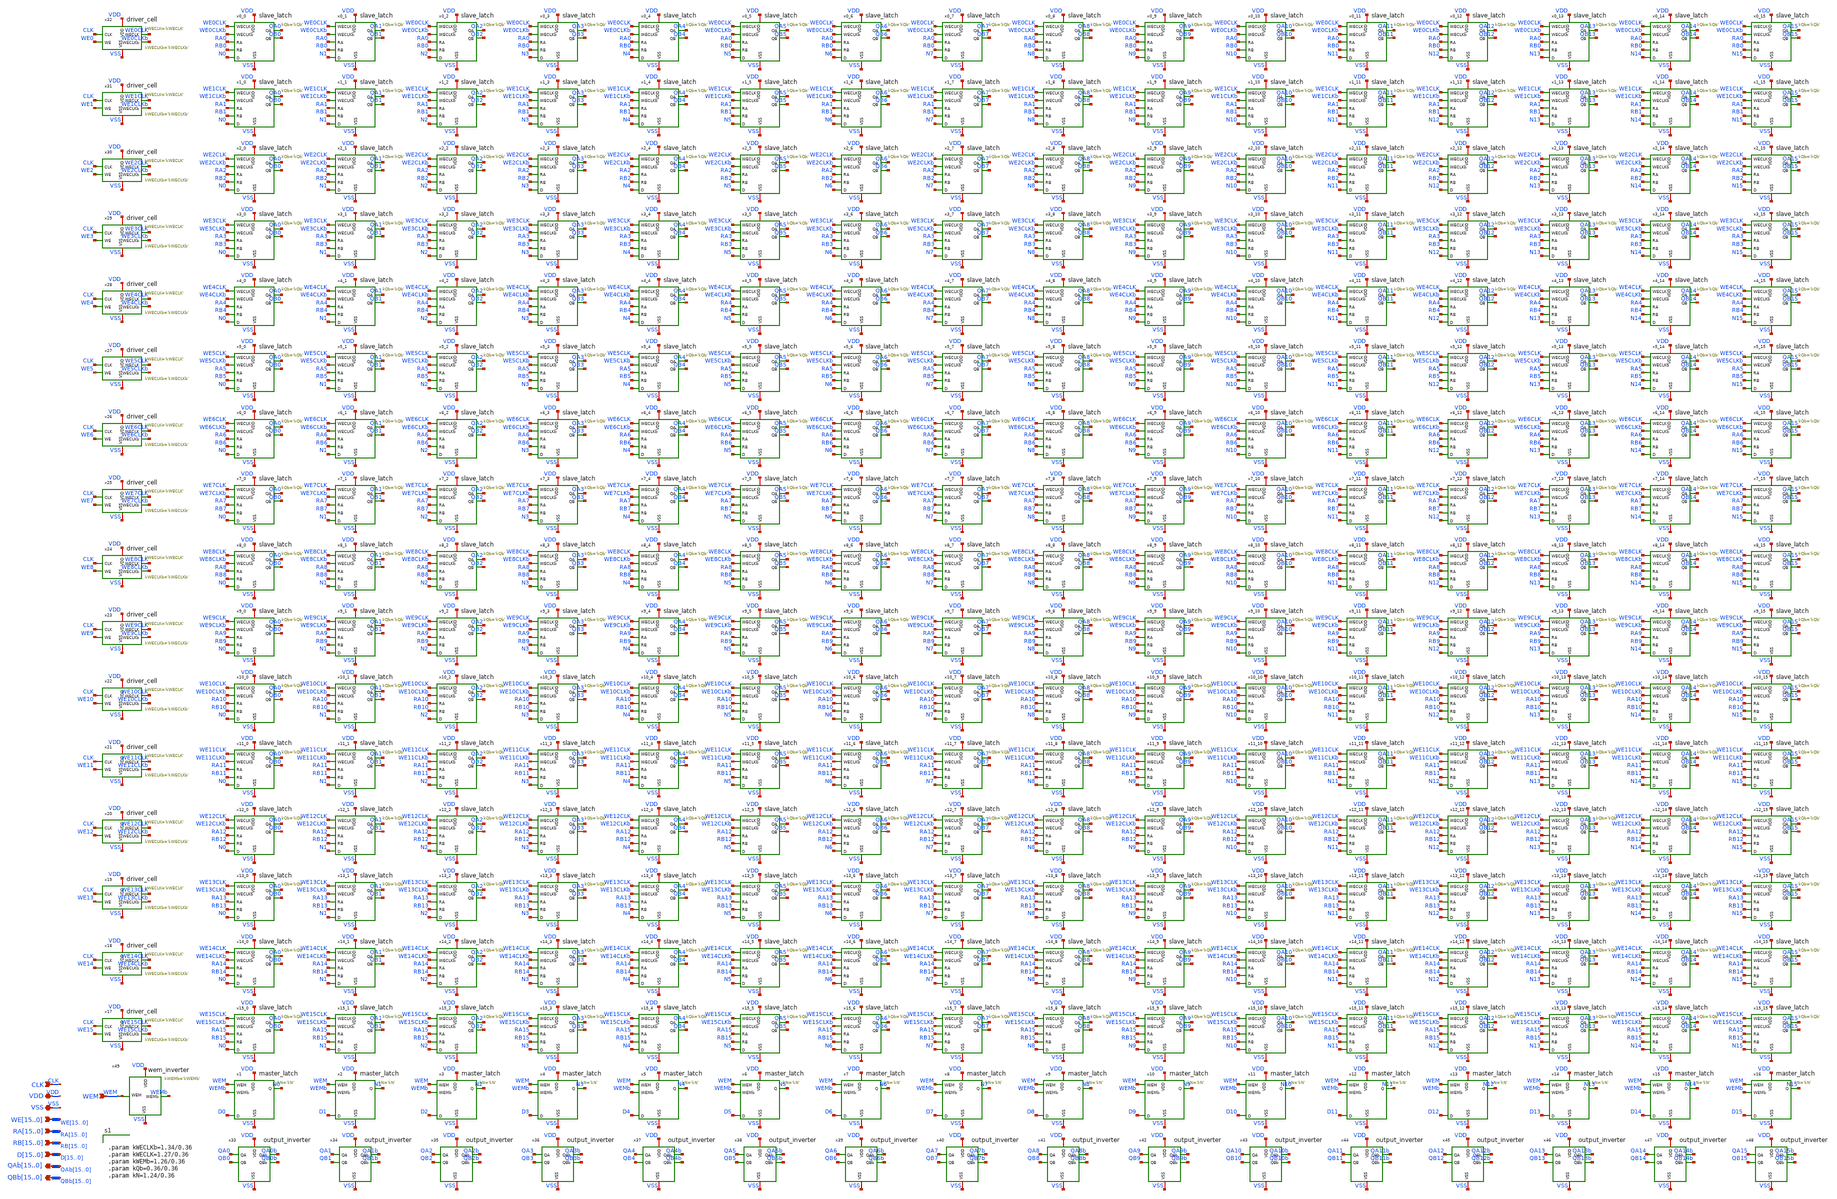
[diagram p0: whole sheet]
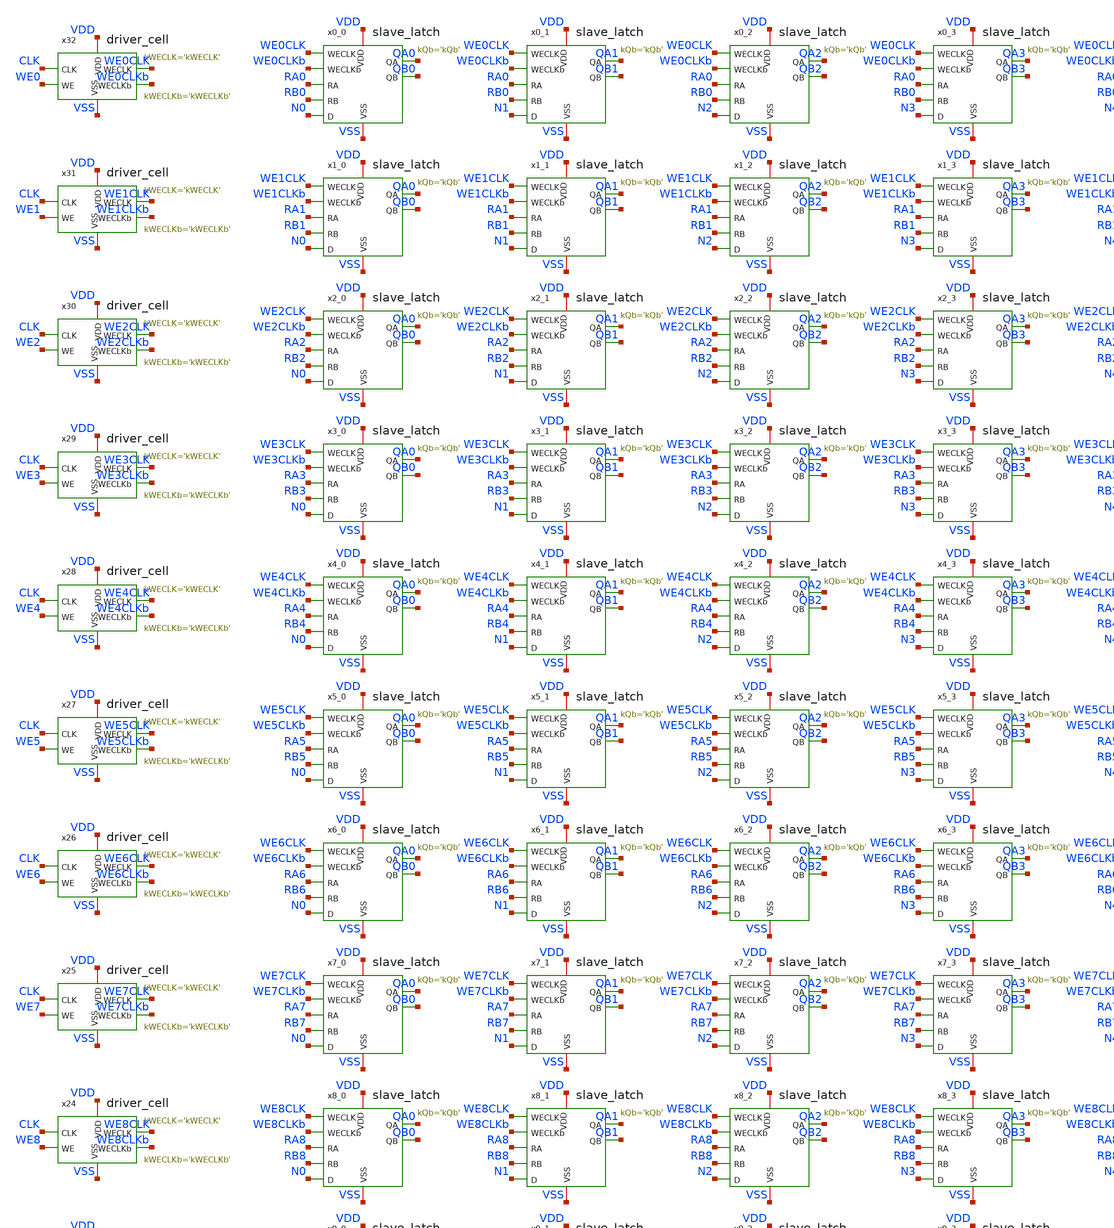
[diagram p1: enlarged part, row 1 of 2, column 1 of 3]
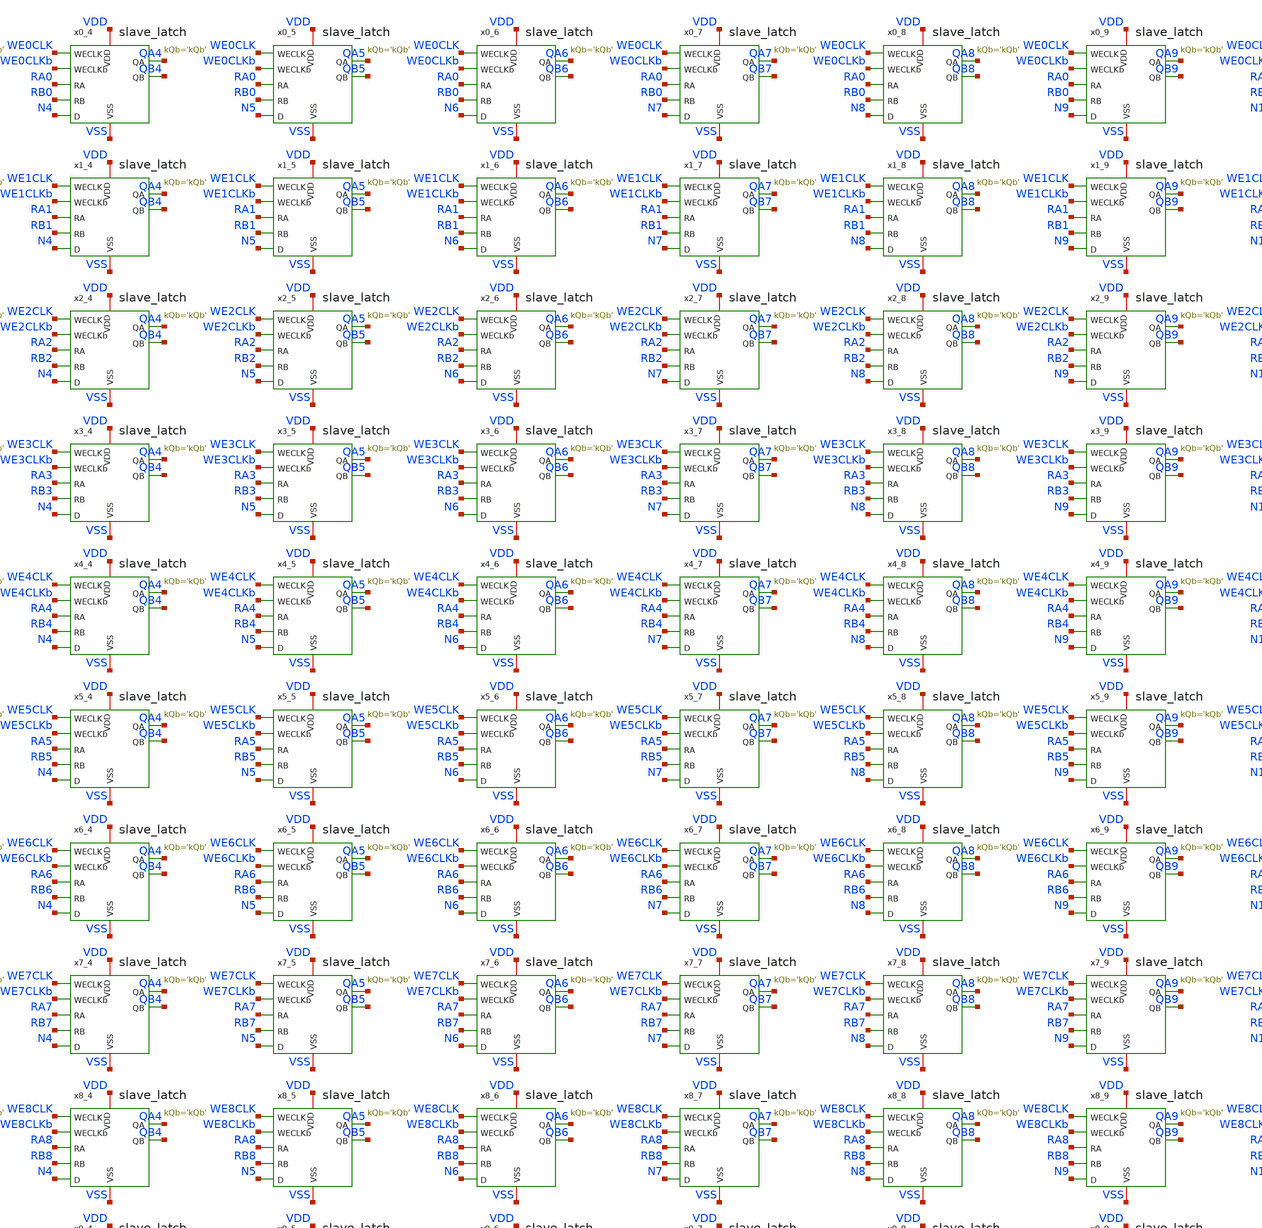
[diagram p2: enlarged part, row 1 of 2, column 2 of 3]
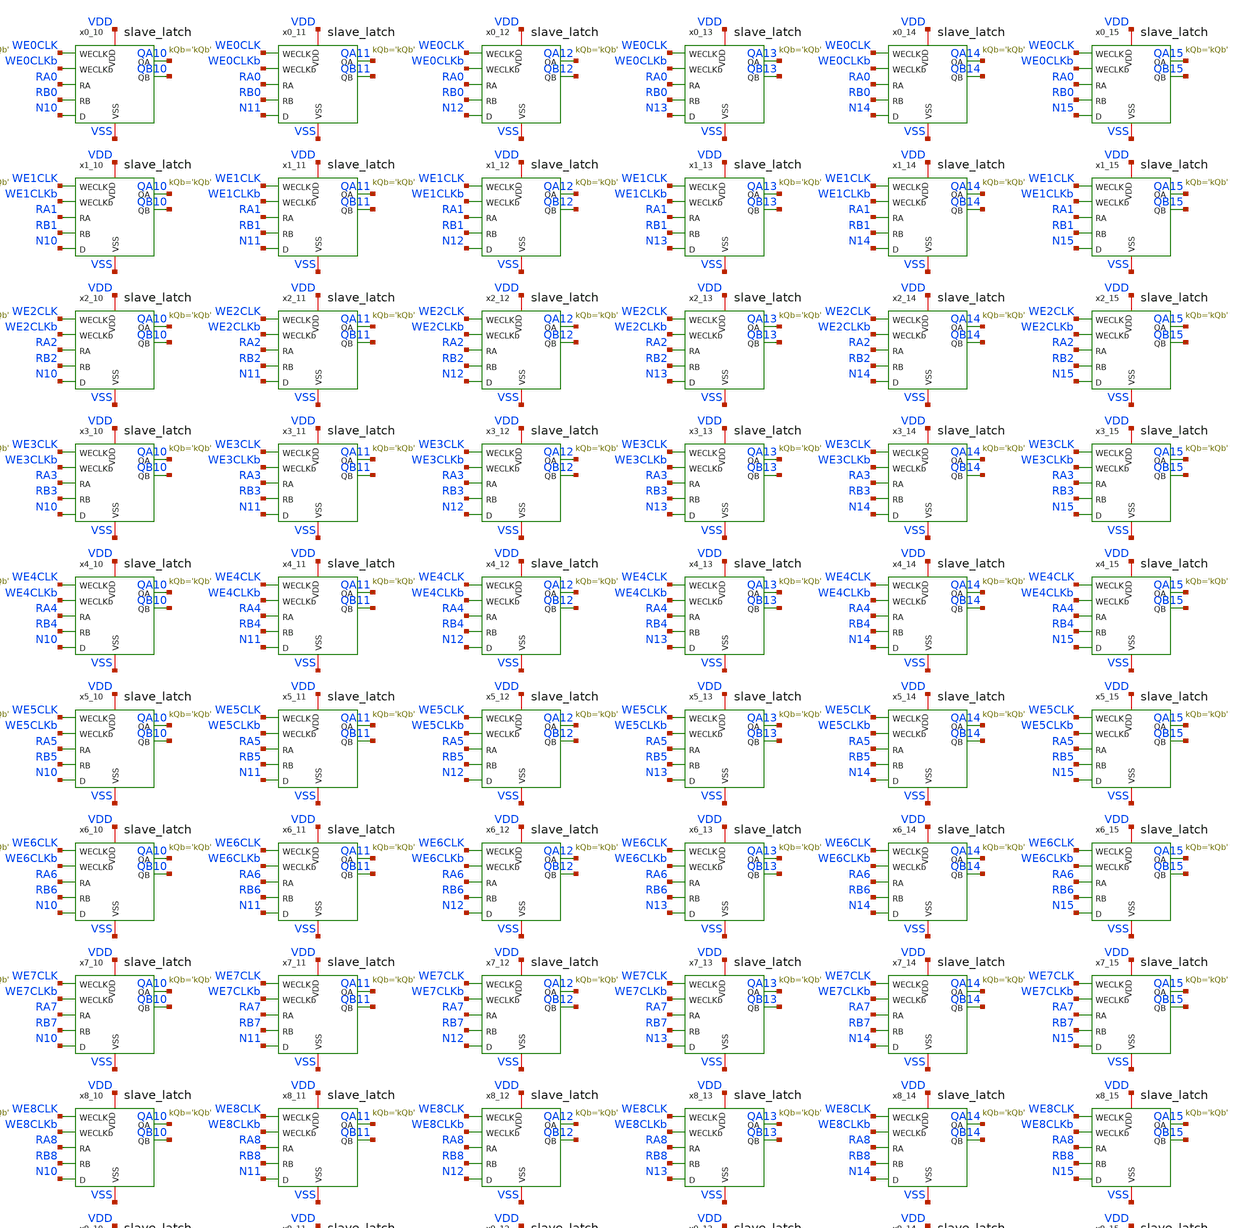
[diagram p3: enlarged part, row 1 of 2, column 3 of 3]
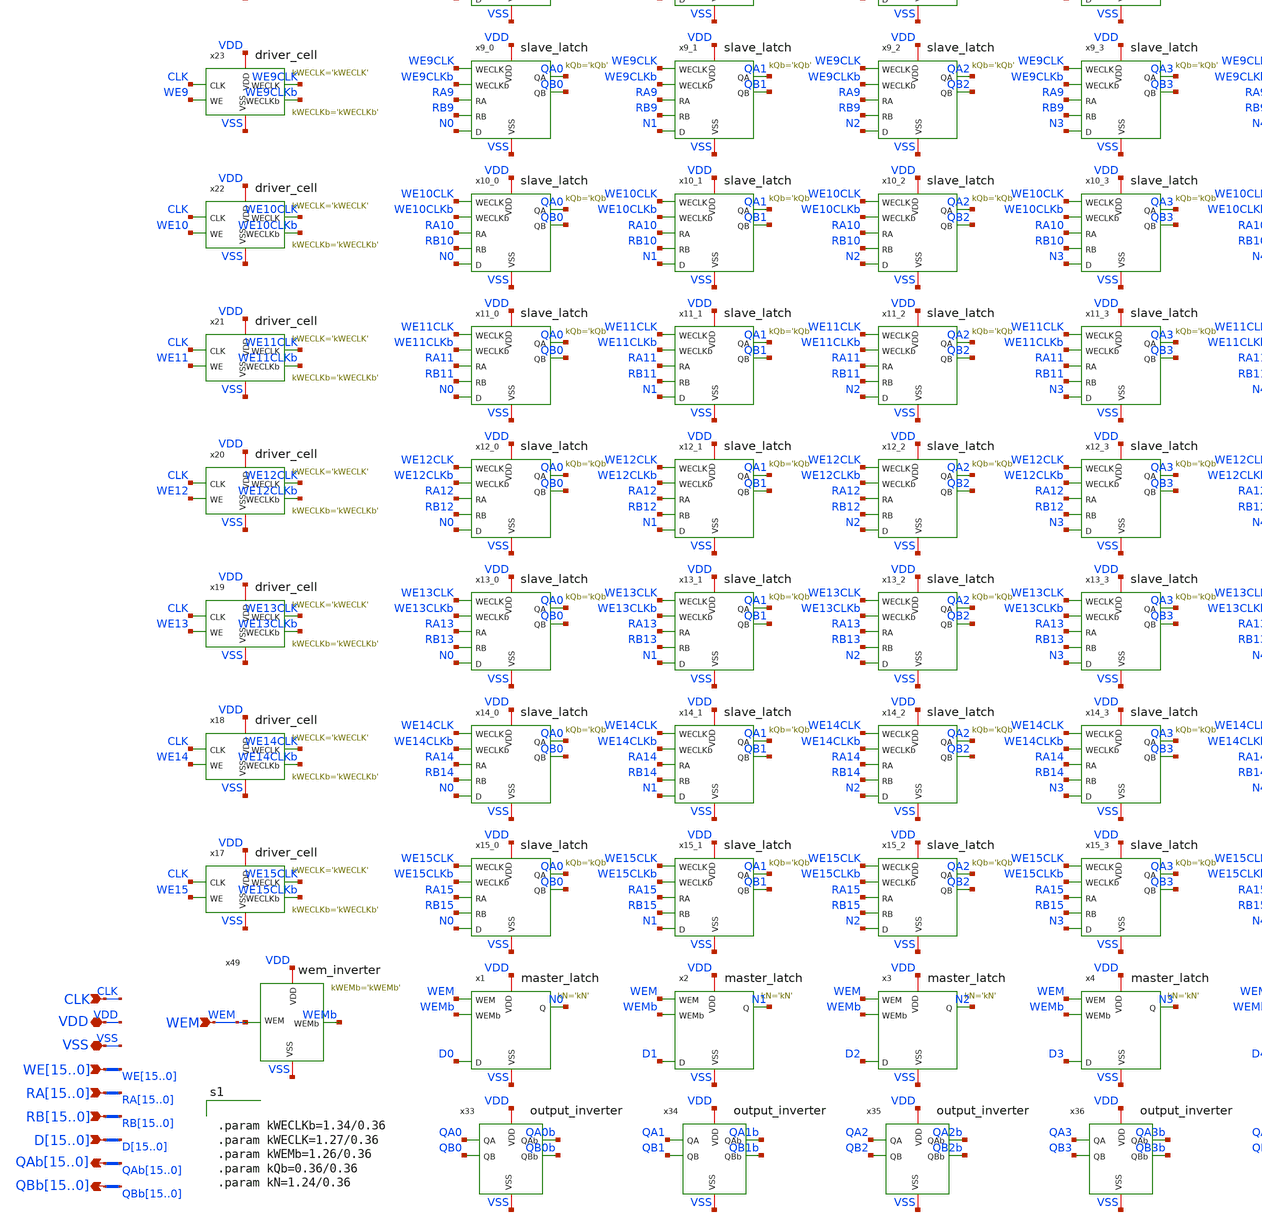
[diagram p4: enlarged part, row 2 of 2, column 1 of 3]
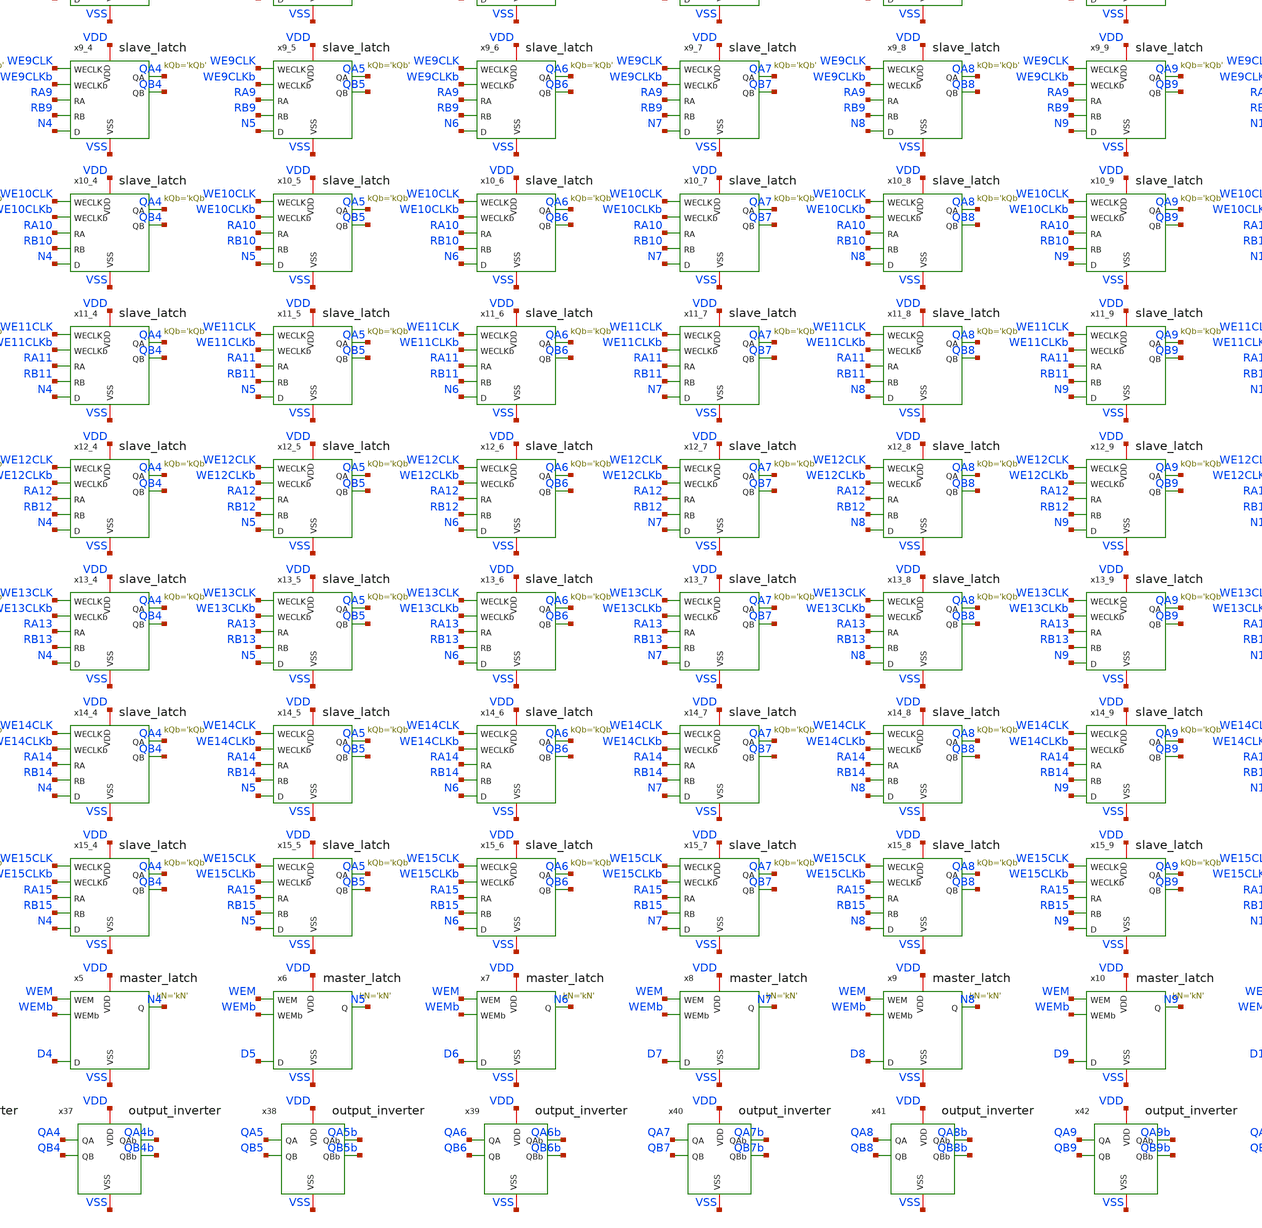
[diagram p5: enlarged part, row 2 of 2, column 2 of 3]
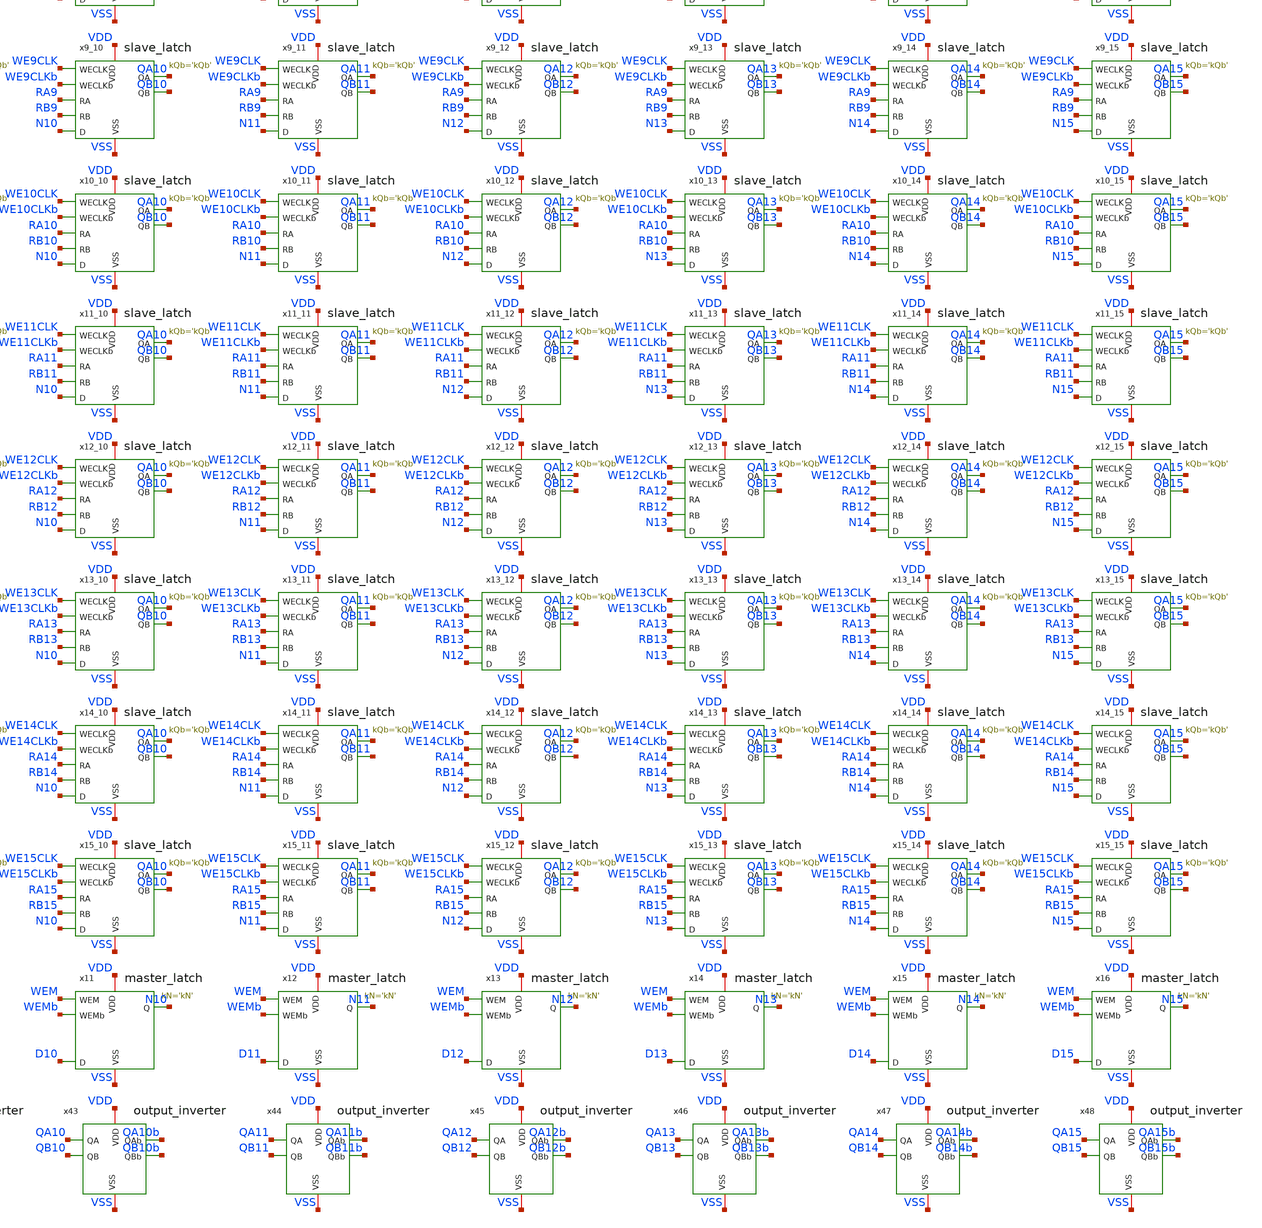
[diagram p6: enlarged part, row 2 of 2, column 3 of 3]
** sch_path: CAD3/rf.sch
**.subckt rf RA15,RA14,RA13,RA12,RA11,RA10,RA9,RA8,RA7,RA6,RA5,RA4,RA3,RA2,RA1,RA0
*+ RB15,RB14,RB13,RB12,RB11,RB10,RB9,RB8,RB7,RB6,RB5,RB4,RB3,RB2,RB1,RB0 WE15,WE14,WE13,WE12,WE11,WE10,WE9,WE8,WE7,WE6,WE5,WE4,WE3,WE2,WE1,WE0 CLK WEM
*+ D15,D14,D13,D12,D11,D10,D9,D8,D7,D6,D5,D4,D3,D2,D1,D0 VDD VSS QAb15,QAb14,QAb13,QAb12,QAb11,QAb10,QAb9,QAb8,QAb7,QAb6,QAb5,QAb4,QAb3,QAb2,QAb1,QAb0
*+ QBb15,QBb14,QBb13,QBb12,QBb11,QBb10,QBb9,QBb8,QBb7,QBb6,QBb5,QBb4,QBb3,QBb2,QBb1,QBb0
*.ipin RA15,RA14,RA13,RA12,RA11,RA10,RA9,RA8,RA7,RA6,RA5,RA4,RA3,RA2,RA1,RA0
*.ipin RB15,RB14,RB13,RB12,RB11,RB10,RB9,RB8,RB7,RB6,RB5,RB4,RB3,RB2,RB1,RB0
*.ipin WE15,WE14,WE13,WE12,WE11,WE10,WE9,WE8,WE7,WE6,WE5,WE4,WE3,WE2,WE1,WE0
*.ipin CLK
*.ipin WEM
*.ipin D15,D14,D13,D12,D11,D10,D9,D8,D7,D6,D5,D4,D3,D2,D1,D0
*.iopin VDD
*.iopin VSS
*.opin QAb15,QAb14,QAb13,QAb12,QAb11,QAb10,QAb9,QAb8,QAb7,QAb6,QAb5,QAb4,QAb3,QAb2,QAb1,QAb0
*.opin QBb15,QBb14,QBb13,QBb12,QBb11,QBb10,QBb9,QBb8,QBb7,QBb6,QBb5,QBb4,QBb3,QBb2,QBb1,QBb0
x0_0 VDD VSS QA0 WE0CLK WE0CLKb RA0 RB0 QB0 N0 slave_latch kQb='kQb'
x0_1 VDD VSS QA1 WE0CLK WE0CLKb RA0 RB0 QB1 N1 slave_latch kQb='kQb'
x0_2 VDD VSS QA2 WE0CLK WE0CLKb RA0 RB0 QB2 N2 slave_latch kQb='kQb'
x0_3 VDD VSS QA3 WE0CLK WE0CLKb RA0 RB0 QB3 N3 slave_latch kQb='kQb'
x0_4 VDD VSS QA4 WE0CLK WE0CLKb RA0 RB0 QB4 N4 slave_latch kQb='kQb'
x0_5 VDD VSS QA5 WE0CLK WE0CLKb RA0 RB0 QB5 N5 slave_latch kQb='kQb'
x0_6 VDD VSS QA6 WE0CLK WE0CLKb RA0 RB0 QB6 N6 slave_latch kQb='kQb'
x0_7 VDD VSS QA7 WE0CLK WE0CLKb RA0 RB0 QB7 N7 slave_latch kQb='kQb'
x0_8 VDD VSS QA8 WE0CLK WE0CLKb RA0 RB0 QB8 N8 slave_latch kQb='kQb'
x0_9 VDD VSS QA9 WE0CLK WE0CLKb RA0 RB0 QB9 N9 slave_latch kQb='kQb'
x0_10 VDD VSS QA10 WE0CLK WE0CLKb RA0 RB0 QB10 N10 slave_latch kQb='kQb'
x0_11 VDD VSS QA11 WE0CLK WE0CLKb RA0 RB0 QB11 N11 slave_latch kQb='kQb'
x0_12 VDD VSS QA12 WE0CLK WE0CLKb RA0 RB0 QB12 N12 slave_latch kQb='kQb'
x0_13 VDD VSS QA13 WE0CLK WE0CLKb RA0 RB0 QB13 N13 slave_latch kQb='kQb'
x0_14 VDD VSS QA14 WE0CLK WE0CLKb RA0 RB0 QB14 N14 slave_latch kQb='kQb'
x0_15 VDD VSS QA15 WE0CLK WE0CLKb RA0 RB0 QB15 N15 slave_latch kQb='kQb'
x1_0 VDD VSS QA0 WE1CLK WE1CLKb RA1 RB1 QB0 N0 slave_latch kQb='kQb'
x1_1 VDD VSS QA1 WE1CLK WE1CLKb RA1 RB1 QB1 N1 slave_latch kQb='kQb'
x1_2 VDD VSS QA2 WE1CLK WE1CLKb RA1 RB1 QB2 N2 slave_latch kQb='kQb'
x1_3 VDD VSS QA3 WE1CLK WE1CLKb RA1 RB1 QB3 N3 slave_latch kQb='kQb'
x1_4 VDD VSS QA4 WE1CLK WE1CLKb RA1 RB1 QB4 N4 slave_latch kQb='kQb'
x1_5 VDD VSS QA5 WE1CLK WE1CLKb RA1 RB1 QB5 N5 slave_latch kQb='kQb'
x1_6 VDD VSS QA6 WE1CLK WE1CLKb RA1 RB1 QB6 N6 slave_latch kQb='kQb'
x1_7 VDD VSS QA7 WE1CLK WE1CLKb RA1 RB1 QB7 N7 slave_latch kQb='kQb'
x1_8 VDD VSS QA8 WE1CLK WE1CLKb RA1 RB1 QB8 N8 slave_latch kQb='kQb'
x1_9 VDD VSS QA9 WE1CLK WE1CLKb RA1 RB1 QB9 N9 slave_latch kQb='kQb'
x1_10 VDD VSS QA10 WE1CLK WE1CLKb RA1 RB1 QB10 N10 slave_latch kQb='kQb'
x1_11 VDD VSS QA11 WE1CLK WE1CLKb RA1 RB1 QB11 N11 slave_latch kQb='kQb'
x1_12 VDD VSS QA12 WE1CLK WE1CLKb RA1 RB1 QB12 N12 slave_latch kQb='kQb'
x1_13 VDD VSS QA13 WE1CLK WE1CLKb RA1 RB1 QB13 N13 slave_latch kQb='kQb'
x1_14 VDD VSS QA14 WE1CLK WE1CLKb RA1 RB1 QB14 N14 slave_latch kQb='kQb'
x1_15 VDD VSS QA15 WE1CLK WE1CLKb RA1 RB1 QB15 N15 slave_latch kQb='kQb'
x2_0 VDD VSS QA0 WE2CLK WE2CLKb RA2 RB2 QB0 N0 slave_latch kQb='kQb'
x2_1 VDD VSS QA1 WE2CLK WE2CLKb RA2 RB2 QB1 N1 slave_latch kQb='kQb'
x2_2 VDD VSS QA2 WE2CLK WE2CLKb RA2 RB2 QB2 N2 slave_latch kQb='kQb'
x2_3 VDD VSS QA3 WE2CLK WE2CLKb RA2 RB2 QB3 N3 slave_latch kQb='kQb'
x2_4 VDD VSS QA4 WE2CLK WE2CLKb RA2 RB2 QB4 N4 slave_latch kQb='kQb'
x2_5 VDD VSS QA5 WE2CLK WE2CLKb RA2 RB2 QB5 N5 slave_latch kQb='kQb'
x2_6 VDD VSS QA6 WE2CLK WE2CLKb RA2 RB2 QB6 N6 slave_latch kQb='kQb'
x2_7 VDD VSS QA7 WE2CLK WE2CLKb RA2 RB2 QB7 N7 slave_latch kQb='kQb'
x2_8 VDD VSS QA8 WE2CLK WE2CLKb RA2 RB2 QB8 N8 slave_latch kQb='kQb'
x2_9 VDD VSS QA9 WE2CLK WE2CLKb RA2 RB2 QB9 N9 slave_latch kQb='kQb'
x2_10 VDD VSS QA10 WE2CLK WE2CLKb RA2 RB2 QB10 N10 slave_latch kQb='kQb'
x2_11 VDD VSS QA11 WE2CLK WE2CLKb RA2 RB2 QB11 N11 slave_latch kQb='kQb'
x2_12 VDD VSS QA12 WE2CLK WE2CLKb RA2 RB2 QB12 N12 slave_latch kQb='kQb'
x2_13 VDD VSS QA13 WE2CLK WE2CLKb RA2 RB2 QB13 N13 slave_latch kQb='kQb'
x2_14 VDD VSS QA14 WE2CLK WE2CLKb RA2 RB2 QB14 N14 slave_latch kQb='kQb'
x2_15 VDD VSS QA15 WE2CLK WE2CLKb RA2 RB2 QB15 N15 slave_latch kQb='kQb'
x3_0 VDD VSS QA0 WE3CLK WE3CLKb RA3 RB3 QB0 N0 slave_latch kQb='kQb'
x3_1 VDD VSS QA1 WE3CLK WE3CLKb RA3 RB3 QB1 N1 slave_latch kQb='kQb'
x3_2 VDD VSS QA2 WE3CLK WE3CLKb RA3 RB3 QB2 N2 slave_latch kQb='kQb'
x3_3 VDD VSS QA3 WE3CLK WE3CLKb RA3 RB3 QB3 N3 slave_latch kQb='kQb'
x3_4 VDD VSS QA4 WE3CLK WE3CLKb RA3 RB3 QB4 N4 slave_latch kQb='kQb'
x3_5 VDD VSS QA5 WE3CLK WE3CLKb RA3 RB3 QB5 N5 slave_latch kQb='kQb'
x3_6 VDD VSS QA6 WE3CLK WE3CLKb RA3 RB3 QB6 N6 slave_latch kQb='kQb'
x3_7 VDD VSS QA7 WE3CLK WE3CLKb RA3 RB3 QB7 N7 slave_latch kQb='kQb'
x3_8 VDD VSS QA8 WE3CLK WE3CLKb RA3 RB3 QB8 N8 slave_latch kQb='kQb'
x3_9 VDD VSS QA9 WE3CLK WE3CLKb RA3 RB3 QB9 N9 slave_latch kQb='kQb'
x3_10 VDD VSS QA10 WE3CLK WE3CLKb RA3 RB3 QB10 N10 slave_latch kQb='kQb'
x3_11 VDD VSS QA11 WE3CLK WE3CLKb RA3 RB3 QB11 N11 slave_latch kQb='kQb'
x3_12 VDD VSS QA12 WE3CLK WE3CLKb RA3 RB3 QB12 N12 slave_latch kQb='kQb'
x3_13 VDD VSS QA13 WE3CLK WE3CLKb RA3 RB3 QB13 N13 slave_latch kQb='kQb'
x3_14 VDD VSS QA14 WE3CLK WE3CLKb RA3 RB3 QB14 N14 slave_latch kQb='kQb'
x3_15 VDD VSS QA15 WE3CLK WE3CLKb RA3 RB3 QB15 N15 slave_latch kQb='kQb'
x4_0 VDD VSS QA0 WE4CLK WE4CLKb RA4 RB4 QB0 N0 slave_latch kQb='kQb'
x4_1 VDD VSS QA1 WE4CLK WE4CLKb RA4 RB4 QB1 N1 slave_latch kQb='kQb'
x4_2 VDD VSS QA2 WE4CLK WE4CLKb RA4 RB4 QB2 N2 slave_latch kQb='kQb'
x4_3 VDD VSS QA3 WE4CLK WE4CLKb RA4 RB4 QB3 N3 slave_latch kQb='kQb'
x4_4 VDD VSS QA4 WE4CLK WE4CLKb RA4 RB4 QB4 N4 slave_latch kQb='kQb'
x4_5 VDD VSS QA5 WE4CLK WE4CLKb RA4 RB4 QB5 N5 slave_latch kQb='kQb'
x4_6 VDD VSS QA6 WE4CLK WE4CLKb RA4 RB4 QB6 N6 slave_latch kQb='kQb'
x4_7 VDD VSS QA7 WE4CLK WE4CLKb RA4 RB4 QB7 N7 slave_latch kQb='kQb'
x4_8 VDD VSS QA8 WE4CLK WE4CLKb RA4 RB4 QB8 N8 slave_latch kQb='kQb'
x4_9 VDD VSS QA9 WE4CLK WE4CLKb RA4 RB4 QB9 N9 slave_latch kQb='kQb'
x4_10 VDD VSS QA10 WE4CLK WE4CLKb RA4 RB4 QB10 N10 slave_latch kQb='kQb'
x4_11 VDD VSS QA11 WE4CLK WE4CLKb RA4 RB4 QB11 N11 slave_latch kQb='kQb'
x4_12 VDD VSS QA12 WE4CLK WE4CLKb RA4 RB4 QB12 N12 slave_latch kQb='kQb'
x4_13 VDD VSS QA13 WE4CLK WE4CLKb RA4 RB4 QB13 N13 slave_latch kQb='kQb'
x4_14 VDD VSS QA14 WE4CLK WE4CLKb RA4 RB4 QB14 N14 slave_latch kQb='kQb'
x4_15 VDD VSS QA15 WE4CLK WE4CLKb RA4 RB4 QB15 N15 slave_latch kQb='kQb'
x5_0 VDD VSS QA0 WE5CLK WE5CLKb RA5 RB5 QB0 N0 slave_latch kQb='kQb'
x5_1 VDD VSS QA1 WE5CLK WE5CLKb RA5 RB5 QB1 N1 slave_latch kQb='kQb'
x5_2 VDD VSS QA2 WE5CLK WE5CLKb RA5 RB5 QB2 N2 slave_latch kQb='kQb'
x5_3 VDD VSS QA3 WE5CLK WE5CLKb RA5 RB5 QB3 N3 slave_latch kQb='kQb'
x5_4 VDD VSS QA4 WE5CLK WE5CLKb RA5 RB5 QB4 N4 slave_latch kQb='kQb'
x5_5 VDD VSS QA5 WE5CLK WE5CLKb RA5 RB5 QB5 N5 slave_latch kQb='kQb'
x5_6 VDD VSS QA6 WE5CLK WE5CLKb RA5 RB5 QB6 N6 slave_latch kQb='kQb'
x5_7 VDD VSS QA7 WE5CLK WE5CLKb RA5 RB5 QB7 N7 slave_latch kQb='kQb'
x5_8 VDD VSS QA8 WE5CLK WE5CLKb RA5 RB5 QB8 N8 slave_latch kQb='kQb'
x5_9 VDD VSS QA9 WE5CLK WE5CLKb RA5 RB5 QB9 N9 slave_latch kQb='kQb'
x5_10 VDD VSS QA10 WE5CLK WE5CLKb RA5 RB5 QB10 N10 slave_latch kQb='kQb'
x5_11 VDD VSS QA11 WE5CLK WE5CLKb RA5 RB5 QB11 N11 slave_latch kQb='kQb'
x5_12 VDD VSS QA12 WE5CLK WE5CLKb RA5 RB5 QB12 N12 slave_latch kQb='kQb'
x5_13 VDD VSS QA13 WE5CLK WE5CLKb RA5 RB5 QB13 N13 slave_latch kQb='kQb'
x5_14 VDD VSS QA14 WE5CLK WE5CLKb RA5 RB5 QB14 N14 slave_latch kQb='kQb'
x5_15 VDD VSS QA15 WE5CLK WE5CLKb RA5 RB5 QB15 N15 slave_latch kQb='kQb'
x6_0 VDD VSS QA0 WE6CLK WE6CLKb RA6 RB6 QB0 N0 slave_latch kQb='kQb'
x6_1 VDD VSS QA1 WE6CLK WE6CLKb RA6 RB6 QB1 N1 slave_latch kQb='kQb'
x6_2 VDD VSS QA2 WE6CLK WE6CLKb RA6 RB6 QB2 N2 slave_latch kQb='kQb'
x6_3 VDD VSS QA3 WE6CLK WE6CLKb RA6 RB6 QB3 N3 slave_latch kQb='kQb'
x6_4 VDD VSS QA4 WE6CLK WE6CLKb RA6 RB6 QB4 N4 slave_latch kQb='kQb'
x6_5 VDD VSS QA5 WE6CLK WE6CLKb RA6 RB6 QB5 N5 slave_latch kQb='kQb'
x6_6 VDD VSS QA6 WE6CLK WE6CLKb RA6 RB6 QB6 N6 slave_latch kQb='kQb'
x6_7 VDD VSS QA7 WE6CLK WE6CLKb RA6 RB6 QB7 N7 slave_latch kQb='kQb'
x6_8 VDD VSS QA8 WE6CLK WE6CLKb RA6 RB6 QB8 N8 slave_latch kQb='kQb'
x6_9 VDD VSS QA9 WE6CLK WE6CLKb RA6 RB6 QB9 N9 slave_latch kQb='kQb'
x6_10 VDD VSS QA10 WE6CLK WE6CLKb RA6 RB6 QB10 N10 slave_latch kQb='kQb'
x6_11 VDD VSS QA11 WE6CLK WE6CLKb RA6 RB6 QB11 N11 slave_latch kQb='kQb'
x6_12 VDD VSS QA12 WE6CLK WE6CLKb RA6 RB6 QB12 N12 slave_latch kQb='kQb'
x6_13 VDD VSS QA13 WE6CLK WE6CLKb RA6 RB6 QB13 N13 slave_latch kQb='kQb'
x6_14 VDD VSS QA14 WE6CLK WE6CLKb RA6 RB6 QB14 N14 slave_latch kQb='kQb'
x6_15 VDD VSS QA15 WE6CLK WE6CLKb RA6 RB6 QB15 N15 slave_latch kQb='kQb'
x7_0 VDD VSS QA0 WE7CLK WE7CLKb RA7 RB7 QB0 N0 slave_latch kQb='kQb'
x7_1 VDD VSS QA1 WE7CLK WE7CLKb RA7 RB7 QB1 N1 slave_latch kQb='kQb'
x7_2 VDD VSS QA2 WE7CLK WE7CLKb RA7 RB7 QB2 N2 slave_latch kQb='kQb'
x7_3 VDD VSS QA3 WE7CLK WE7CLKb RA7 RB7 QB3 N3 slave_latch kQb='kQb'
x7_4 VDD VSS QA4 WE7CLK WE7CLKb RA7 RB7 QB4 N4 slave_latch kQb='kQb'
x7_5 VDD VSS QA5 WE7CLK WE7CLKb RA7 RB7 QB5 N5 slave_latch kQb='kQb'
x7_6 VDD VSS QA6 WE7CLK WE7CLKb RA7 RB7 QB6 N6 slave_latch kQb='kQb'
x7_7 VDD VSS QA7 WE7CLK WE7CLKb RA7 RB7 QB7 N7 slave_latch kQb='kQb'
x7_8 VDD VSS QA8 WE7CLK WE7CLKb RA7 RB7 QB8 N8 slave_latch kQb='kQb'
x7_9 VDD VSS QA9 WE7CLK WE7CLKb RA7 RB7 QB9 N9 slave_latch kQb='kQb'
x7_10 VDD VSS QA10 WE7CLK WE7CLKb RA7 RB7 QB10 N10 slave_latch kQb='kQb'
x7_11 VDD VSS QA11 WE7CLK WE7CLKb RA7 RB7 QB11 N11 slave_latch kQb='kQb'
x7_12 VDD VSS QA12 WE7CLK WE7CLKb RA7 RB7 QB12 N12 slave_latch kQb='kQb'
x7_13 VDD VSS QA13 WE7CLK WE7CLKb RA7 RB7 QB13 N13 slave_latch kQb='kQb'
x7_14 VDD VSS QA14 WE7CLK WE7CLKb RA7 RB7 QB14 N14 slave_latch kQb='kQb'
x7_15 VDD VSS QA15 WE7CLK WE7CLKb RA7 RB7 QB15 N15 slave_latch kQb='kQb'
x8_0 VDD VSS QA0 WE8CLK WE8CLKb RA8 RB8 QB0 N0 slave_latch kQb='kQb'
x8_1 VDD VSS QA1 WE8CLK WE8CLKb RA8 RB8 QB1 N1 slave_latch kQb='kQb'
x8_2 VDD VSS QA2 WE8CLK WE8CLKb RA8 RB8 QB2 N2 slave_latch kQb='kQb'
x8_3 VDD VSS QA3 WE8CLK WE8CLKb RA8 RB8 QB3 N3 slave_latch kQb='kQb'
x8_4 VDD VSS QA4 WE8CLK WE8CLKb RA8 RB8 QB4 N4 slave_latch kQb='kQb'
x8_5 VDD VSS QA5 WE8CLK WE8CLKb RA8 RB8 QB5 N5 slave_latch kQb='kQb'
x8_6 VDD VSS QA6 WE8CLK WE8CLKb RA8 RB8 QB6 N6 slave_latch kQb='kQb'
x8_7 VDD VSS QA7 WE8CLK WE8CLKb RA8 RB8 QB7 N7 slave_latch kQb='kQb'
x8_8 VDD VSS QA8 WE8CLK WE8CLKb RA8 RB8 QB8 N8 slave_latch kQb='kQb'
x8_9 VDD VSS QA9 WE8CLK WE8CLKb RA8 RB8 QB9 N9 slave_latch kQb='kQb'
x8_10 VDD VSS QA10 WE8CLK WE8CLKb RA8 RB8 QB10 N10 slave_latch kQb='kQb'
x8_11 VDD VSS QA11 WE8CLK WE8CLKb RA8 RB8 QB11 N11 slave_latch kQb='kQb'
x8_12 VDD VSS QA12 WE8CLK WE8CLKb RA8 RB8 QB12 N12 slave_latch kQb='kQb'
x8_13 VDD VSS QA13 WE8CLK WE8CLKb RA8 RB8 QB13 N13 slave_latch kQb='kQb'
x8_14 VDD VSS QA14 WE8CLK WE8CLKb RA8 RB8 QB14 N14 slave_latch kQb='kQb'
x8_15 VDD VSS QA15 WE8CLK WE8CLKb RA8 RB8 QB15 N15 slave_latch kQb='kQb'
x9_0 VDD VSS QA0 WE9CLK WE9CLKb RA9 RB9 QB0 N0 slave_latch kQb='kQb'
x9_1 VDD VSS QA1 WE9CLK WE9CLKb RA9 RB9 QB1 N1 slave_latch kQb='kQb'
x9_2 VDD VSS QA2 WE9CLK WE9CLKb RA9 RB9 QB2 N2 slave_latch kQb='kQb'
x9_3 VDD VSS QA3 WE9CLK WE9CLKb RA9 RB9 QB3 N3 slave_latch kQb='kQb'
x9_4 VDD VSS QA4 WE9CLK WE9CLKb RA9 RB9 QB4 N4 slave_latch kQb='kQb'
x9_5 VDD VSS QA5 WE9CLK WE9CLKb RA9 RB9 QB5 N5 slave_latch kQb='kQb'
x9_6 VDD VSS QA6 WE9CLK WE9CLKb RA9 RB9 QB6 N6 slave_latch kQb='kQb'
x9_7 VDD VSS QA7 WE9CLK WE9CLKb RA9 RB9 QB7 N7 slave_latch kQb='kQb'
x9_8 VDD VSS QA8 WE9CLK WE9CLKb RA9 RB9 QB8 N8 slave_latch kQb='kQb'
x9_9 VDD VSS QA9 WE9CLK WE9CLKb RA9 RB9 QB9 N9 slave_latch kQb='kQb'
x9_10 VDD VSS QA10 WE9CLK WE9CLKb RA9 RB9 QB10 N10 slave_latch kQb='kQb'
x9_11 VDD VSS QA11 WE9CLK WE9CLKb RA9 RB9 QB11 N11 slave_latch kQb='kQb'
x9_12 VDD VSS QA12 WE9CLK WE9CLKb RA9 RB9 QB12 N12 slave_latch kQb='kQb'
x9_13 VDD VSS QA13 WE9CLK WE9CLKb RA9 RB9 QB13 N13 slave_latch kQb='kQb'
x9_14 VDD VSS QA14 WE9CLK WE9CLKb RA9 RB9 QB14 N14 slave_latch kQb='kQb'
x9_15 VDD VSS QA15 WE9CLK WE9CLKb RA9 RB9 QB15 N15 slave_latch kQb='kQb'
x10_0 VDD VSS QA0 WE10CLK WE10CLKb RA10 RB10 QB0 N0 slave_latch kQb='kQb'
x10_1 VDD VSS QA1 WE10CLK WE10CLKb RA10 RB10 QB1 N1 slave_latch kQb='kQb'
x10_2 VDD VSS QA2 WE10CLK WE10CLKb RA10 RB10 QB2 N2 slave_latch kQb='kQb'
x10_3 VDD VSS QA3 WE10CLK WE10CLKb RA10 RB10 QB3 N3 slave_latch kQb='kQb'
x10_4 VDD VSS QA4 WE10CLK WE10CLKb RA10 RB10 QB4 N4 slave_latch kQb='kQb'
x10_5 VDD VSS QA5 WE10CLK WE10CLKb RA10 RB10 QB5 N5 slave_latch kQb='kQb'
x10_6 VDD VSS QA6 WE10CLK WE10CLKb RA10 RB10 QB6 N6 slave_latch kQb='kQb'
x10_7 VDD VSS QA7 WE10CLK WE10CLKb RA10 RB10 QB7 N7 slave_latch kQb='kQb'
x10_8 VDD VSS QA8 WE10CLK WE10CLKb RA10 RB10 QB8 N8 slave_latch kQb='kQb'
x10_9 VDD VSS QA9 WE10CLK WE10CLKb RA10 RB10 QB9 N9 slave_latch kQb='kQb'
x10_10 VDD VSS QA10 WE10CLK WE10CLKb RA10 RB10 QB10 N10 slave_latch kQb='kQb'
x10_11 VDD VSS QA11 WE10CLK WE10CLKb RA10 RB10 QB11 N11 slave_latch kQb='kQb'
x10_12 VDD VSS QA12 WE10CLK WE10CLKb RA10 RB10 QB12 N12 slave_latch kQb='kQb'
x10_13 VDD VSS QA13 WE10CLK WE10CLKb RA10 RB10 QB13 N13 slave_latch kQb='kQb'
x10_14 VDD VSS QA14 WE10CLK WE10CLKb RA10 RB10 QB14 N14 slave_latch kQb='kQb'
x10_15 VDD VSS QA15 WE10CLK WE10CLKb RA10 RB10 QB15 N15 slave_latch kQb='kQb'
x11_0 VDD VSS QA0 WE11CLK WE11CLKb RA11 RB11 QB0 N0 slave_latch kQb='kQb'
x11_1 VDD VSS QA1 WE11CLK WE11CLKb RA11 RB11 QB1 N1 slave_latch kQb='kQb'
x11_2 VDD VSS QA2 WE11CLK WE11CLKb RA11 RB11 QB2 N2 slave_latch kQb='kQb'
x11_3 VDD VSS QA3 WE11CLK WE11CLKb RA11 RB11 QB3 N3 slave_latch kQb='kQb'
x11_4 VDD VSS QA4 WE11CLK WE11CLKb RA11 RB11 QB4 N4 slave_latch kQb='kQb'
x11_5 VDD VSS QA5 WE11CLK WE11CLKb RA11 RB11 QB5 N5 slave_latch kQb='kQb'
x11_6 VDD VSS QA6 WE11CLK WE11CLKb RA11 RB11 QB6 N6 slave_latch kQb='kQb'
x11_7 VDD VSS QA7 WE11CLK WE11CLKb RA11 RB11 QB7 N7 slave_latch kQb='kQb'
x11_8 VDD VSS QA8 WE11CLK WE11CLKb RA11 RB11 QB8 N8 slave_latch kQb='kQb'
x11_9 VDD VSS QA9 WE11CLK WE11CLKb RA11 RB11 QB9 N9 slave_latch kQb='kQb'
x11_10 VDD VSS QA10 WE11CLK WE11CLKb RA11 RB11 QB10 N10 slave_latch kQb='kQb'
x11_11 VDD VSS QA11 WE11CLK WE11CLKb RA11 RB11 QB11 N11 slave_latch kQb='kQb'
x11_12 VDD VSS QA12 WE11CLK WE11CLKb RA11 RB11 QB12 N12 slave_latch kQb='kQb'
x11_13 VDD VSS QA13 WE11CLK WE11CLKb RA11 RB11 QB13 N13 slave_latch kQb='kQb'
x11_14 VDD VSS QA14 WE11CLK WE11CLKb RA11 RB11 QB14 N14 slave_latch kQb='kQb'
x11_15 VDD VSS QA15 WE11CLK WE11CLKb RA11 RB11 QB15 N15 slave_latch kQb='kQb'
x12_0 VDD VSS QA0 WE12CLK WE12CLKb RA12 RB12 QB0 N0 slave_latch kQb='kQb'
x12_1 VDD VSS QA1 WE12CLK WE12CLKb RA12 RB12 QB1 N1 slave_latch kQb='kQb'
x12_2 VDD VSS QA2 WE12CLK WE12CLKb RA12 RB12 QB2 N2 slave_latch kQb='kQb'
x12_3 VDD VSS QA3 WE12CLK WE12CLKb RA12 RB12 QB3 N3 slave_latch kQb='kQb'
x12_4 VDD VSS QA4 WE12CLK WE12CLKb RA12 RB12 QB4 N4 slave_latch kQb='kQb'
x12_5 VDD VSS QA5 WE12CLK WE12CLKb RA12 RB12 QB5 N5 slave_latch kQb='kQb'
x12_6 VDD VSS QA6 WE12CLK WE12CLKb RA12 RB12 QB6 N6 slave_latch kQb='kQb'
x12_7 VDD VSS QA7 WE12CLK WE12CLKb RA12 RB12 QB7 N7 slave_latch kQb='kQb'
x12_8 VDD VSS QA8 WE12CLK WE12CLKb RA12 RB12 QB8 N8 slave_latch kQb='kQb'
x12_9 VDD VSS QA9 WE12CLK WE12CLKb RA12 RB12 QB9 N9 slave_latch kQb='kQb'
x12_10 VDD VSS QA10 WE12CLK WE12CLKb RA12 RB12 QB10 N10 slave_latch kQb='kQb'
x12_11 VDD VSS QA11 WE12CLK WE12CLKb RA12 RB12 QB11 N11 slave_latch kQb='kQb'
x12_12 VDD VSS QA12 WE12CLK WE12CLKb RA12 RB12 QB12 N12 slave_latch kQb='kQb'
x12_13 VDD VSS QA13 WE12CLK WE12CLKb RA12 RB12 QB13 N13 slave_latch kQb='kQb'
x12_14 VDD VSS QA14 WE12CLK WE12CLKb RA12 RB12 QB14 N14 slave_latch kQb='kQb'
x12_15 VDD VSS QA15 WE12CLK WE12CLKb RA12 RB12 QB15 N15 slave_latch kQb='kQb'
x13_0 VDD VSS QA0 WE13CLK WE13CLKb RA13 RB13 QB0 N0 slave_latch kQb='kQb'
x13_1 VDD VSS QA1 WE13CLK WE13CLKb RA13 RB13 QB1 N1 slave_latch kQb='kQb'
x13_2 VDD VSS QA2 WE13CLK WE13CLKb RA13 RB13 QB2 N2 slave_latch kQb='kQb'
x13_3 VDD VSS QA3 WE13CLK WE13CLKb RA13 RB13 QB3 N3 slave_latch kQb='kQb'
x13_4 VDD VSS QA4 WE13CLK WE13CLKb RA13 RB13 QB4 N4 slave_latch kQb='kQb'
x13_5 VDD VSS QA5 WE13CLK WE13CLKb RA13 RB13 QB5 N5 slave_latch kQb='kQb'
x13_6 VDD VSS QA6 WE13CLK WE13CLKb RA13 RB13 QB6 N6 slave_latch kQb='kQb'
x13_7 VDD VSS QA7 WE13CLK WE13CLKb RA13 RB13 QB7 N7 slave_latch kQb='kQb'
x13_8 VDD VSS QA8 WE13CLK WE13CLKb RA13 RB13 QB8 N8 slave_latch kQb='kQb'
x13_9 VDD VSS QA9 WE13CLK WE13CLKb RA13 RB13 QB9 N9 slave_latch kQb='kQb'
x13_10 VDD VSS QA10 WE13CLK WE13CLKb RA13 RB13 QB10 N10 slave_latch kQb='kQb'
x13_11 VDD VSS QA11 WE13CLK WE13CLKb RA13 RB13 QB11 N11 slave_latch kQb='kQb'
x13_12 VDD VSS QA12 WE13CLK WE13CLKb RA13 RB13 QB12 N12 slave_latch kQb='kQb'
x13_13 VDD VSS QA13 WE13CLK WE13CLKb RA13 RB13 QB13 N13 slave_latch kQb='kQb'
x13_14 VDD VSS QA14 WE13CLK WE13CLKb RA13 RB13 QB14 N14 slave_latch kQb='kQb'
x13_15 VDD VSS QA15 WE13CLK WE13CLKb RA13 RB13 QB15 N15 slave_latch kQb='kQb'
x14_0 VDD VSS QA0 WE14CLK WE14CLKb RA14 RB14 QB0 N0 slave_latch kQb='kQb'
x14_1 VDD VSS QA1 WE14CLK WE14CLKb RA14 RB14 QB1 N1 slave_latch kQb='kQb'
x14_2 VDD VSS QA2 WE14CLK WE14CLKb RA14 RB14 QB2 N2 slave_latch kQb='kQb'
x14_3 VDD VSS QA3 WE14CLK WE14CLKb RA14 RB14 QB3 N3 slave_latch kQb='kQb'
x14_4 VDD VSS QA4 WE14CLK WE14CLKb RA14 RB14 QB4 N4 slave_latch kQb='kQb'
x14_5 VDD VSS QA5 WE14CLK WE14CLKb RA14 RB14 QB5 N5 slave_latch kQb='kQb'
x14_6 VDD VSS QA6 WE14CLK WE14CLKb RA14 RB14 QB6 N6 slave_latch kQb='kQb'
x14_7 VDD VSS QA7 WE14CLK WE14CLKb RA14 RB14 QB7 N7 slave_latch kQb='kQb'
x14_8 VDD VSS QA8 WE14CLK WE14CLKb RA14 RB14 QB8 N8 slave_latch kQb='kQb'
x14_9 VDD VSS QA9 WE14CLK WE14CLKb RA14 RB14 QB9 N9 slave_latch kQb='kQb'
x14_10 VDD VSS QA10 WE14CLK WE14CLKb RA14 RB14 QB10 N10 slave_latch kQb='kQb'
x14_11 VDD VSS QA11 WE14CLK WE14CLKb RA14 RB14 QB11 N11 slave_latch kQb='kQb'
x14_12 VDD VSS QA12 WE14CLK WE14CLKb RA14 RB14 QB12 N12 slave_latch kQb='kQb'
x14_13 VDD VSS QA13 WE14CLK WE14CLKb RA14 RB14 QB13 N13 slave_latch kQb='kQb'
x14_14 VDD VSS QA14 WE14CLK WE14CLKb RA14 RB14 QB14 N14 slave_latch kQb='kQb'
x14_15 VDD VSS QA15 WE14CLK WE14CLKb RA14 RB14 QB15 N15 slave_latch kQb='kQb'
x15_0 VDD VSS QA0 WE15CLK WE15CLKb RA15 RB15 QB0 N0 slave_latch kQb='kQb'
x15_1 VDD VSS QA1 WE15CLK WE15CLKb RA15 RB15 QB1 N1 slave_latch kQb='kQb'
x15_2 VDD VSS QA2 WE15CLK WE15CLKb RA15 RB15 QB2 N2 slave_latch kQb='kQb'
x15_3 VDD VSS QA3 WE15CLK WE15CLKb RA15 RB15 QB3 N3 slave_latch kQb='kQb'
x15_4 VDD VSS QA4 WE15CLK WE15CLKb RA15 RB15 QB4 N4 slave_latch kQb='kQb'
x15_5 VDD VSS QA5 WE15CLK WE15CLKb RA15 RB15 QB5 N5 slave_latch kQb='kQb'
x15_6 VDD VSS QA6 WE15CLK WE15CLKb RA15 RB15 QB6 N6 slave_latch kQb='kQb'
x15_7 VDD VSS QA7 WE15CLK WE15CLKb RA15 RB15 QB7 N7 slave_latch kQb='kQb'
x15_8 VDD VSS QA8 WE15CLK WE15CLKb RA15 RB15 QB8 N8 slave_latch kQb='kQb'
x15_9 VDD VSS QA9 WE15CLK WE15CLKb RA15 RB15 QB9 N9 slave_latch kQb='kQb'
x15_10 VDD VSS QA10 WE15CLK WE15CLKb RA15 RB15 QB10 N10 slave_latch kQb='kQb'
x15_11 VDD VSS QA11 WE15CLK WE15CLKb RA15 RB15 QB11 N11 slave_latch kQb='kQb'
x15_12 VDD VSS QA12 WE15CLK WE15CLKb RA15 RB15 QB12 N12 slave_latch kQb='kQb'
x15_13 VDD VSS QA13 WE15CLK WE15CLKb RA15 RB15 QB13 N13 slave_latch kQb='kQb'
x15_14 VDD VSS QA14 WE15CLK WE15CLKb RA15 RB15 QB14 N14 slave_latch kQb='kQb'
x15_15 VDD VSS QA15 WE15CLK WE15CLKb RA15 RB15 QB15 N15 slave_latch kQb='kQb'
x1 VDD VSS N0 WEM WEMb D0 master_latch kN='kN'
x2 VDD VSS N1 WEM WEMb D1 master_latch kN='kN'
x3 VDD VSS N2 WEM WEMb D2 master_latch kN='kN'
x4 VDD VSS N3 WEM WEMb D3 master_latch kN='kN'
x5 VDD VSS N4 WEM WEMb D4 master_latch kN='kN'
x6 VDD VSS N5 WEM WEMb D5 master_latch kN='kN'
x7 VDD VSS N6 WEM WEMb D6 master_latch kN='kN'
x8 VDD VSS N7 WEM WEMb D7 master_latch kN='kN'
x9 VDD VSS N8 WEM WEMb D8 master_latch kN='kN'
x10 VDD VSS N9 WEM WEMb D9 master_latch kN='kN'
x11 VDD VSS N10 WEM WEMb D10 master_latch kN='kN'
x12 VDD VSS N11 WEM WEMb D11 master_latch kN='kN'
x13 VDD VSS N12 WEM WEMb D12 master_latch kN='kN'
x14 VDD VSS N13 WEM WEMb D13 master_latch kN='kN'
x15 VDD VSS N14 WEM WEMb D14 master_latch kN='kN'
x16 VDD VSS N15 WEM WEMb D15 master_latch kN='kN'
x17 CLK WE15 WE15CLKb VDD VSS WE15CLK driver_cell kWECLK='kWECLK' kWECLKb='kWECLKb'
x18 CLK WE14 WE14CLKb VDD VSS WE14CLK driver_cell kWECLK='kWECLK' kWECLKb='kWECLKb'
x19 CLK WE13 WE13CLKb VDD VSS WE13CLK driver_cell kWECLK='kWECLK' kWECLKb='kWECLKb'
x20 CLK WE12 WE12CLKb VDD VSS WE12CLK driver_cell kWECLK='kWECLK' kWECLKb='kWECLKb'
x21 CLK WE11 WE11CLKb VDD VSS WE11CLK driver_cell kWECLK='kWECLK' kWECLKb='kWECLKb'
x22 CLK WE10 WE10CLKb VDD VSS WE10CLK driver_cell kWECLK='kWECLK' kWECLKb='kWECLKb'
x23 CLK WE9 WE9CLKb VDD VSS WE9CLK driver_cell kWECLK='kWECLK' kWECLKb='kWECLKb'
x24 CLK WE8 WE8CLKb VDD VSS WE8CLK driver_cell kWECLK='kWECLK' kWECLKb='kWECLKb'
x25 CLK WE7 WE7CLKb VDD VSS WE7CLK driver_cell kWECLK='kWECLK' kWECLKb='kWECLKb'
x26 CLK WE6 WE6CLKb VDD VSS WE6CLK driver_cell kWECLK='kWECLK' kWECLKb='kWECLKb'
x27 CLK WE5 WE5CLKb VDD VSS WE5CLK driver_cell kWECLK='kWECLK' kWECLKb='kWECLKb'
x28 CLK WE4 WE4CLKb VDD VSS WE4CLK driver_cell kWECLK='kWECLK' kWECLKb='kWECLKb'
x29 CLK WE3 WE3CLKb VDD VSS WE3CLK driver_cell kWECLK='kWECLK' kWECLKb='kWECLKb'
x30 CLK WE2 WE2CLKb VDD VSS WE2CLK driver_cell kWECLK='kWECLK' kWECLKb='kWECLKb'
x31 CLK WE1 WE1CLKb VDD VSS WE1CLK driver_cell kWECLK='kWECLK' kWECLKb='kWECLKb'
x32 CLK WE0 WE0CLKb VDD VSS WE0CLK driver_cell kWECLK='kWECLK' kWECLKb='kWECLKb'
x33 VDD VSS QA0b QA0 QB0 QB0b output_inverter
x34 VDD VSS QA1b QA1 QB1 QB1b output_inverter
x35 VDD VSS QA2b QA2 QB2 QB2b output_inverter
x36 VDD VSS QA3b QA3 QB3 QB3b output_inverter
x37 VDD VSS QA4b QA4 QB4 QB4b output_inverter
x38 VDD VSS QA5b QA5 QB5 QB5b output_inverter
x39 VDD VSS QA6b QA6 QB6 QB6b output_inverter
x40 VDD VSS QA7b QA7 QB7 QB7b output_inverter
x41 VDD VSS QA8b QA8 QB8 QB8b output_inverter
x42 VDD VSS QA9b QA9 QB9 QB9b output_inverter
x43 VDD VSS QA10b QA10 QB10 QB10b output_inverter
x44 VDD VSS QA11b QA11 QB11 QB11b output_inverter
x45 VDD VSS QA12b QA12 QB12 QB12b output_inverter
x46 VDD VSS QA13b QA13 QB13 QB13b output_inverter
x47 VDD VSS QA14b QA14 QB14 QB14b output_inverter
x48 VDD VSS QA15b QA15 QB15 QB15b output_inverter
x49 VDD WEM WEMb VSS wem_inverter
**** begin user architecture code


.param kWECLKb=1.34/0.36
.param kWECLK=1.27/0.36
.param kWEMb=1.26/0.36
.param kQb=0.36/0.36
.param kN=1.24/0.36


**** end user architecture code
**.ends

* expanding   symbol:  engn1600-team1/CAD3/slave_latch.sym # of pins=9
** sym_path: CAD3/slave_latch.sym
** sch_path: CAD3/slave_latch.sch
.subckt slave_latch VDD VSS QA WECLK WECLKb RA RB QB D  kQb=1
*.ipin D
*.ipin RA
*.ipin RB
*.ipin WECLKb
*.ipin WECLK
*.opin QA
*.opin QB
*.iopin VDD
*.iopin VSS
XM1 net1 WECLKb net2 VDD pfet_03v3 L=0.28u W=0.36u nf=1 ad='int((nf+1)/2) * W/nf * 0.18u' as='int((nf+2)/2) * W/nf * 0.18u'
+ pd='2*int((nf+1)/2) * (W/nf + 0.18u)' ps='2*int((nf+2)/2) * (W/nf + 0.18u)' nrd='0.18u / W' nrs='0.18u / W'
+ sa=0 sb=0 sd=0 m=1
XM2 net1 D VDD VDD pfet_03v3 L=0.28u W=0.72u nf=1 ad='int((nf+1)/2) * W/nf * 0.18u' as='int((nf+2)/2) * W/nf * 0.18u'
+ pd='2*int((nf+1)/2) * (W/nf + 0.18u)' ps='2*int((nf+2)/2) * (W/nf + 0.18u)' nrd='0.18u / W' nrs='0.18u / W'
+ sa=0 sb=0 sd=0 m=1
XM3 net3 net2 VDD VDD pfet_03v3 L=0.28u W=0.72u nf=1 ad='int((nf+1)/2) * W/nf * 0.18u' as='int((nf+2)/2) * W/nf * 0.18u'
+ pd='2*int((nf+1)/2) * (W/nf + 0.18u)' ps='2*int((nf+2)/2) * (W/nf + 0.18u)' nrd='0.18u / W' nrs='0.18u / W'
+ sa=0 sb=0 sd=0 m=1
XM4 net4 net2 VDD VDD pfet_03v3 L=0.28u W=0.36u nf=1 ad='int((nf+1)/2) * W/nf * 0.18u' as='int((nf+2)/2) * W/nf * 0.18u'
+ pd='2*int((nf+1)/2) * (W/nf + 0.18u)' ps='2*int((nf+2)/2) * (W/nf + 0.18u)' nrd='0.18u / W' nrs='0.18u / W'
+ sa=0 sb=0 sd=0 m=1
XM5 VDD WECLK net8 VDD pfet_03v3 L=0.28u W=0.36u nf=1 ad='int((nf+1)/2) * W/nf * 0.18u' as='int((nf+2)/2) * W/nf * 0.18u'
+ pd='2*int((nf+1)/2) * (W/nf + 0.18u)' ps='2*int((nf+2)/2) * (W/nf + 0.18u)' nrd='0.18u / W' nrs='0.18u / W'
+ sa=0 sb=0 sd=0 m=1
XM6 net8 net4 net2 VDD pfet_03v3 L=0.28u W=0.36u nf=1 ad='int((nf+1)/2) * W/nf * 0.18u' as='int((nf+2)/2) * W/nf * 0.18u'
+ pd='2*int((nf+1)/2) * (W/nf + 0.18u)' ps='2*int((nf+2)/2) * (W/nf + 0.18u)' nrd='0.18u / W' nrs='0.18u / W'
+ sa=0 sb=0 sd=0 m=1
XM7 net1 D VSS VSS nfet_03v3 L=0.28u W=0.36u nf=1 ad='int((nf+1)/2) * W/nf * 0.18u' as='int((nf+2)/2) * W/nf * 0.18u'
+ pd='2*int((nf+1)/2) * (W/nf + 0.18u)' ps='2*int((nf+2)/2) * (W/nf + 0.18u)' nrd='0.18u / W' nrs='0.18u / W'
+ sa=0 sb=0 sd=0 m=1
XM8 net1 WECLK net2 VSS nfet_03v3 L=0.28u W=0.36u nf=1 ad='int((nf+1)/2) * W/nf * 0.18u' as='int((nf+2)/2) * W/nf * 0.18u'
+ pd='2*int((nf+1)/2) * (W/nf + 0.18u)' ps='2*int((nf+2)/2) * (W/nf + 0.18u)' nrd='0.18u / W' nrs='0.18u / W'
+ sa=0 sb=0 sd=0 m=1
XM9 net3 net2 VSS VSS nfet_03v3 L=0.28u W=0.36u nf=1 ad='int((nf+1)/2) * W/nf * 0.18u' as='int((nf+2)/2) * W/nf * 0.18u'
+ pd='2*int((nf+1)/2) * (W/nf + 0.18u)' ps='2*int((nf+2)/2) * (W/nf + 0.18u)' nrd='0.18u / W' nrs='0.18u / W'
+ sa=0 sb=0 sd=0 m=1
XM10 net4 net2 VSS VSS nfet_03v3 L=0.28u W=0.36u nf=1 ad='int((nf+1)/2) * W/nf * 0.18u' as='int((nf+2)/2) * W/nf * 0.18u'
+ pd='2*int((nf+1)/2) * (W/nf + 0.18u)' ps='2*int((nf+2)/2) * (W/nf + 0.18u)' nrd='0.18u / W' nrs='0.18u / W'
+ sa=0 sb=0 sd=0 m=1
XM11 net7 net4 net2 VSS nfet_03v3 L=0.28u W=0.36u nf=1 ad='int((nf+1)/2) * W/nf * 0.18u' as='int((nf+2)/2) * W/nf * 0.18u'
+ pd='2*int((nf+1)/2) * (W/nf + 0.18u)' ps='2*int((nf+2)/2) * (W/nf + 0.18u)' nrd='0.18u / W' nrs='0.18u / W'
+ sa=0 sb=0 sd=0 m=1
XM12 VSS WECLKb net7 VSS nfet_03v3 L=0.28u W=0.36u nf=1 ad='int((nf+1)/2) * W/nf * 0.18u' as='int((nf+2)/2) * W/nf * 0.18u'
+ pd='2*int((nf+1)/2) * (W/nf + 0.18u)' ps='2*int((nf+2)/2) * (W/nf + 0.18u)' nrd='0.18u / W' nrs='0.18u / W'
+ sa=0 sb=0 sd=0 m=1
XM13 net3 net5 QB VDD pfet_03v3 L=0.28u W='kQb*0.36u' nf=1 ad='int((nf+1)/2) * W/nf * 0.18u' as='int((nf+2)/2) * W/nf * 0.18u'
+ pd='2*int((nf+1)/2) * (W/nf + 0.18u)' ps='2*int((nf+2)/2) * (W/nf + 0.18u)' nrd='0.18u / W' nrs='0.18u / W'
+ sa=0 sb=0 sd=0 m=1
XM14 net3 RB QB VSS nfet_03v3 L=0.28u W='kQb*0.36u' nf=1 ad='int((nf+1)/2) * W/nf * 0.18u' as='int((nf+2)/2) * W/nf * 0.18u'
+ pd='2*int((nf+1)/2) * (W/nf + 0.18u)' ps='2*int((nf+2)/2) * (W/nf + 0.18u)' nrd='0.18u / W' nrs='0.18u / W'
+ sa=0 sb=0 sd=0 m=1
XM15 net5 RB VDD VDD pfet_03v3 L=0.28u W=0.72u nf=1 ad='int((nf+1)/2) * W/nf * 0.18u' as='int((nf+2)/2) * W/nf * 0.18u'
+ pd='2*int((nf+1)/2) * (W/nf + 0.18u)' ps='2*int((nf+2)/2) * (W/nf + 0.18u)' nrd='0.18u / W' nrs='0.18u / W'
+ sa=0 sb=0 sd=0 m=1
XM16 net5 RB VSS VSS nfet_03v3 L=0.28u W=0.36u nf=1 ad='int((nf+1)/2) * W/nf * 0.18u' as='int((nf+2)/2) * W/nf * 0.18u'
+ pd='2*int((nf+1)/2) * (W/nf + 0.18u)' ps='2*int((nf+2)/2) * (W/nf + 0.18u)' nrd='0.18u / W' nrs='0.18u / W'
+ sa=0 sb=0 sd=0 m=1
XM21 net3 net6 QA VDD pfet_03v3 L=0.28u W='kQb*0.36u' nf=1 ad='int((nf+1)/2) * W/nf * 0.18u' as='int((nf+2)/2) * W/nf * 0.18u'
+ pd='2*int((nf+1)/2) * (W/nf + 0.18u)' ps='2*int((nf+2)/2) * (W/nf + 0.18u)' nrd='0.18u / W' nrs='0.18u / W'
+ sa=0 sb=0 sd=0 m=1
XM22 net3 RA QA VSS nfet_03v3 L=0.28u W='kQb*0.36u' nf=1 ad='int((nf+1)/2) * W/nf * 0.18u' as='int((nf+2)/2) * W/nf * 0.18u'
+ pd='2*int((nf+1)/2) * (W/nf + 0.18u)' ps='2*int((nf+2)/2) * (W/nf + 0.18u)' nrd='0.18u / W' nrs='0.18u / W'
+ sa=0 sb=0 sd=0 m=1
XM23 net6 RA VDD VDD pfet_03v3 L=0.28u W=0.72u nf=1 ad='int((nf+1)/2) * W/nf * 0.18u' as='int((nf+2)/2) * W/nf * 0.18u'
+ pd='2*int((nf+1)/2) * (W/nf + 0.18u)' ps='2*int((nf+2)/2) * (W/nf + 0.18u)' nrd='0.18u / W' nrs='0.18u / W'
+ sa=0 sb=0 sd=0 m=1
XM24 net6 RA VSS VSS nfet_03v3 L=0.28u W=0.36u nf=1 ad='int((nf+1)/2) * W/nf * 0.18u' as='int((nf+2)/2) * W/nf * 0.18u'
+ pd='2*int((nf+1)/2) * (W/nf + 0.18u)' ps='2*int((nf+2)/2) * (W/nf + 0.18u)' nrd='0.18u / W' nrs='0.18u / W'
+ sa=0 sb=0 sd=0 m=1
**** begin user architecture code


.param kQb=1


**** end user architecture code
.ends


* expanding   symbol:  engn1600-team1/CAD3/master_latch.sym # of pins=6
** sym_path: CAD3/master_latch.sym
** sch_path: CAD3/master_latch.sch
.subckt master_latch VDD VSS Q WEM WEMb D  kN=1
*.ipin D
*.ipin WEMb
*.ipin WEM
*.iopin VSS
*.iopin VDD
*.opin Q
XM3 net1 WEMb net2 VDD pfet_03v3 L=0.28u W=0.36u nf=1 ad='int((nf+1)/2) * W/nf * 0.18u' as='int((nf+2)/2) * W/nf * 0.18u'
+ pd='2*int((nf+1)/2) * (W/nf + 0.18u)' ps='2*int((nf+2)/2) * (W/nf + 0.18u)' nrd='0.18u / W' nrs='0.18u / W'
+ sa=0 sb=0 sd=0 m=1
XM7 net1 D VDD VDD pfet_03v3 L=0.28u W=0.72u nf=1 ad='int((nf+1)/2) * W/nf * 0.18u' as='int((nf+2)/2) * W/nf * 0.18u'
+ pd='2*int((nf+1)/2) * (W/nf + 0.18u)' ps='2*int((nf+2)/2) * (W/nf + 0.18u)' nrd='0.18u / W' nrs='0.18u / W'
+ sa=0 sb=0 sd=0 m=1
XM8 Q net2 VDD VDD pfet_03v3 L=0.28u W=0.72u nf=4 ad='int((nf+1)/2) * W/nf * 0.18u' as='int((nf+2)/2) * W/nf * 0.18u'
+ pd='2*int((nf+1)/2) * (W/nf + 0.18u)' ps='2*int((nf+2)/2) * (W/nf + 0.18u)' nrd='0.18u / W' nrs='0.18u / W'
+ sa=0 sb=0 sd=0 m=1
XM9 net3 net2 VDD VDD pfet_03v3 L=0.28u W=0.36u nf=1 ad='int((nf+1)/2) * W/nf * 0.18u' as='int((nf+2)/2) * W/nf * 0.18u'
+ pd='2*int((nf+1)/2) * (W/nf + 0.18u)' ps='2*int((nf+2)/2) * (W/nf + 0.18u)' nrd='0.18u / W' nrs='0.18u / W'
+ sa=0 sb=0 sd=0 m=1
XM10 VDD WEM net5 VDD pfet_03v3 L=0.28u W=0.36u nf=1 ad='int((nf+1)/2) * W/nf * 0.18u' as='int((nf+2)/2) * W/nf * 0.18u'
+ pd='2*int((nf+1)/2) * (W/nf + 0.18u)' ps='2*int((nf+2)/2) * (W/nf + 0.18u)' nrd='0.18u / W' nrs='0.18u / W'
+ sa=0 sb=0 sd=0 m=1
XM12 net5 net3 net2 VDD pfet_03v3 L=0.28u W=0.36u nf=1 ad='int((nf+1)/2) * W/nf * 0.18u' as='int((nf+2)/2) * W/nf * 0.18u'
+ pd='2*int((nf+1)/2) * (W/nf + 0.18u)' ps='2*int((nf+2)/2) * (W/nf + 0.18u)' nrd='0.18u / W' nrs='0.18u / W'
+ sa=0 sb=0 sd=0 m=1
XM19 net1 D VSS VSS nfet_03v3 L=0.28u W=0.36u nf=1 ad='int((nf+1)/2) * W/nf * 0.18u' as='int((nf+2)/2) * W/nf * 0.18u'
+ pd='2*int((nf+1)/2) * (W/nf + 0.18u)' ps='2*int((nf+2)/2) * (W/nf + 0.18u)' nrd='0.18u / W' nrs='0.18u / W'
+ sa=0 sb=0 sd=0 m=1
XM20 net1 WEM net2 VSS nfet_03v3 L=0.28u W=0.36u nf=1 ad='int((nf+1)/2) * W/nf * 0.18u' as='int((nf+2)/2) * W/nf * 0.18u'
+ pd='2*int((nf+1)/2) * (W/nf + 0.18u)' ps='2*int((nf+2)/2) * (W/nf + 0.18u)' nrd='0.18u / W' nrs='0.18u / W'
+ sa=0 sb=0 sd=0 m=1
XM21 Q net2 VSS VSS nfet_03v3 L=0.28u W=0.36u nf=4 ad='int((nf+1)/2) * W/nf * 0.18u' as='int((nf+2)/2) * W/nf * 0.18u'
+ pd='2*int((nf+1)/2) * (W/nf + 0.18u)' ps='2*int((nf+2)/2) * (W/nf + 0.18u)' nrd='0.18u / W' nrs='0.18u / W'
+ sa=0 sb=0 sd=0 m=1
XM22 net3 net2 VSS VSS nfet_03v3 L=0.28u W=0.36u nf=1 ad='int((nf+1)/2) * W/nf * 0.18u' as='int((nf+2)/2) * W/nf * 0.18u'
+ pd='2*int((nf+1)/2) * (W/nf + 0.18u)' ps='2*int((nf+2)/2) * (W/nf + 0.18u)' nrd='0.18u / W' nrs='0.18u / W'
+ sa=0 sb=0 sd=0 m=1
XM23 net4 net3 net2 VSS nfet_03v3 L=0.28u W=0.36u nf=1 ad='int((nf+1)/2) * W/nf * 0.18u' as='int((nf+2)/2) * W/nf * 0.18u'
+ pd='2*int((nf+1)/2) * (W/nf + 0.18u)' ps='2*int((nf+2)/2) * (W/nf + 0.18u)' nrd='0.18u / W' nrs='0.18u / W'
+ sa=0 sb=0 sd=0 m=1
XM24 VSS WEMb net4 VSS nfet_03v3 L=0.28u W=0.36u nf=1 ad='int((nf+1)/2) * W/nf * 0.18u' as='int((nf+2)/2) * W/nf * 0.18u'
+ pd='2*int((nf+1)/2) * (W/nf + 0.18u)' ps='2*int((nf+2)/2) * (W/nf + 0.18u)' nrd='0.18u / W' nrs='0.18u / W'
+ sa=0 sb=0 sd=0 m=1
.ends


* expanding   symbol:  engn1600-team1/CAD3/driver_cell.sym # of pins=6
** sym_path: CAD3/driver_cell.sym
** sch_path: CAD3/driver_cell.sch
.subckt driver_cell CLK WE WECLKb VDD VSS WECLK  kWECLK=1 kWECLKb=1
*.ipin CLK
*.ipin WE
*.iopin VSS
*.iopin VDD
*.opin WECLKb
*.opin WECLK
XM13 WECLK net1 VDD VDD pfet_03v3 L=0.28u W=2.54u nf=1 ad='int((nf+1)/2) * W/nf * 0.18u' as='int((nf+2)/2) * W/nf * 0.18u'
+ pd='2*int((nf+1)/2) * (W/nf + 0.18u)' ps='2*int((nf+2)/2) * (W/nf + 0.18u)' nrd='0.18u / W' nrs='0.18u / W'
+ sa=0 sb=0 sd=0 m=1
XM14 WECLK net1 VSS VSS nfet_03v3 L=0.28u W=1.27u nf=1 ad='int((nf+1)/2) * W/nf * 0.18u' as='int((nf+2)/2) * W/nf * 0.18u'
+ pd='2*int((nf+1)/2) * (W/nf + 0.18u)' ps='2*int((nf+2)/2) * (W/nf + 0.18u)' nrd='0.18u / W' nrs='0.18u / W'
+ sa=0 sb=0 sd=0 m=1
XM1 WECLKb WECLK VDD VDD pfet_03v3 L=0.28u W=2.68u nf=1 ad='int((nf+1)/2) * W/nf * 0.18u' as='int((nf+2)/2) * W/nf * 0.18u'
+ pd='2*int((nf+1)/2) * (W/nf + 0.18u)' ps='2*int((nf+2)/2) * (W/nf + 0.18u)' nrd='0.18u / W' nrs='0.18u / W'
+ sa=0 sb=0 sd=0 m=1
XM2 WECLKb WECLK VSS VSS nfet_03v3 L=0.28u W=1.34u nf=1 ad='int((nf+1)/2) * W/nf * 0.18u' as='int((nf+2)/2) * W/nf * 0.18u'
+ pd='2*int((nf+1)/2) * (W/nf + 0.18u)' ps='2*int((nf+2)/2) * (W/nf + 0.18u)' nrd='0.18u / W' nrs='0.18u / W'
+ sa=0 sb=0 sd=0 m=1
XM3 net1 CLK VDD VDD pfet_03v3 L=0.28u W=0.72u nf=1 ad='int((nf+1)/2) * W/nf * 0.18u' as='int((nf+2)/2) * W/nf * 0.18u'
+ pd='2*int((nf+1)/2) * (W/nf + 0.18u)' ps='2*int((nf+2)/2) * (W/nf + 0.18u)' nrd='0.18u / W' nrs='0.18u / W'
+ sa=0 sb=0 sd=0 m=1
XM4 net1 WE VDD VDD pfet_03v3 L=0.28u W=0.72u nf=1 ad='int((nf+1)/2) * W/nf * 0.18u' as='int((nf+2)/2) * W/nf * 0.18u'
+ pd='2*int((nf+1)/2) * (W/nf + 0.18u)' ps='2*int((nf+2)/2) * (W/nf + 0.18u)' nrd='0.18u / W' nrs='0.18u / W'
+ sa=0 sb=0 sd=0 m=1
XM5 net2 WE VSS VSS nfet_03v3 L=0.28u W=0.72u nf=1 ad='int((nf+1)/2) * W/nf * 0.18u' as='int((nf+2)/2) * W/nf * 0.18u'
+ pd='2*int((nf+1)/2) * (W/nf + 0.18u)' ps='2*int((nf+2)/2) * (W/nf + 0.18u)' nrd='0.18u / W' nrs='0.18u / W'
+ sa=0 sb=0 sd=0 m=1
XM6 net1 CLK net2 VSS nfet_03v3 L=0.28u W=0.72u nf=1 ad='int((nf+1)/2) * W/nf * 0.18u' as='int((nf+2)/2) * W/nf * 0.18u'
+ pd='2*int((nf+1)/2) * (W/nf + 0.18u)' ps='2*int((nf+2)/2) * (W/nf + 0.18u)' nrd='0.18u / W' nrs='0.18u / W'
+ sa=0 sb=0 sd=0 m=1
.ends


* expanding   symbol:  engn1600-team1/CAD3/output_inverter.sym # of pins=6
** sym_path: CAD3/output_inverter.sym
** sch_path: CAD3/output_inverter.sch
.subckt output_inverter VDD VSS QAb QA QB QBb
*.opin QB
*.opin QA
*.iopin VDD
*.iopin VSS
*.ipin QAb
*.ipin QBb
XM3 QB QBb VDD VDD pfet_03v3 L=0.28u W=0.72u nf=1 ad='int((nf+1)/2) * W/nf * 0.18u' as='int((nf+2)/2) * W/nf * 0.18u'
+ pd='2*int((nf+1)/2) * (W/nf + 0.18u)' ps='2*int((nf+2)/2) * (W/nf + 0.18u)' nrd='0.18u / W' nrs='0.18u / W'
+ sa=0 sb=0 sd=0 m=1
XM4 QB QBb VSS VSS nfet_03v3 L=0.28u W=0.36 nf=1 ad='int((nf+1)/2) * W/nf * 0.18u' as='int((nf+2)/2) * W/nf * 0.18u'
+ pd='2*int((nf+1)/2) * (W/nf + 0.18u)' ps='2*int((nf+2)/2) * (W/nf + 0.18u)' nrd='0.18u / W' nrs='0.18u / W'
+ sa=0 sb=0 sd=0 m=1
XM35 QA QAb VDD VDD pfet_03v3 L=0.28u W=0.72u nf=1 ad='int((nf+1)/2) * W/nf * 0.18u' as='int((nf+2)/2) * W/nf * 0.18u'
+ pd='2*int((nf+1)/2) * (W/nf + 0.18u)' ps='2*int((nf+2)/2) * (W/nf + 0.18u)' nrd='0.18u / W' nrs='0.18u / W'
+ sa=0 sb=0 sd=0 m=1
XM36 QA QAb VSS VSS nfet_03v3 L=0.28u W=0.36u nf=1 ad='int((nf+1)/2) * W/nf * 0.18u' as='int((nf+2)/2) * W/nf * 0.18u'
+ pd='2*int((nf+1)/2) * (W/nf + 0.18u)' ps='2*int((nf+2)/2) * (W/nf + 0.18u)' nrd='0.18u / W' nrs='0.18u / W'
+ sa=0 sb=0 sd=0 m=1
.ends


* expanding   symbol:  engn1600-team1/CAD3/wem_inverter.sym # of pins=4
** sym_path: CAD3/wem_inverter.sym
** sch_path: CAD3/wem_inverter.sch
.subckt wem_inverter VDD WEM WEMb VSS
*.ipin WEM
*.opin WEMb
*.iopin VDD
*.iopin VSS
XM1 WEMb WEM VDD VDD pfet_03v3 L=0.28u W='kWEMb*0.72u' nf=1 ad='int((nf+1)/2) * W/nf * 0.18u' as='int((nf+2)/2) * W/nf * 0.18u'
+ pd='2*int((nf+1)/2) * (W/nf + 0.18u)' ps='2*int((nf+2)/2) * (W/nf + 0.18u)' nrd='0.18u / W' nrs='0.18u / W'
+ sa=0 sb=0 sd=0 m=1
XM2 WEMb WEM VSS VSS nfet_03v3 L=0.28u W='kWEMb*0.36u' nf=1 ad='int((nf+1)/2) * W/nf * 0.18u' as='int((nf+2)/2) * W/nf * 0.18u'
+ pd='2*int((nf+1)/2) * (W/nf + 0.18u)' ps='2*int((nf+2)/2) * (W/nf + 0.18u)' nrd='0.18u / W' nrs='0.18u / W'
+ sa=0 sb=0 sd=0 m=1
**** begin user architecture code


.param kWEMb=1


**** end user architecture code
.ends

.end
